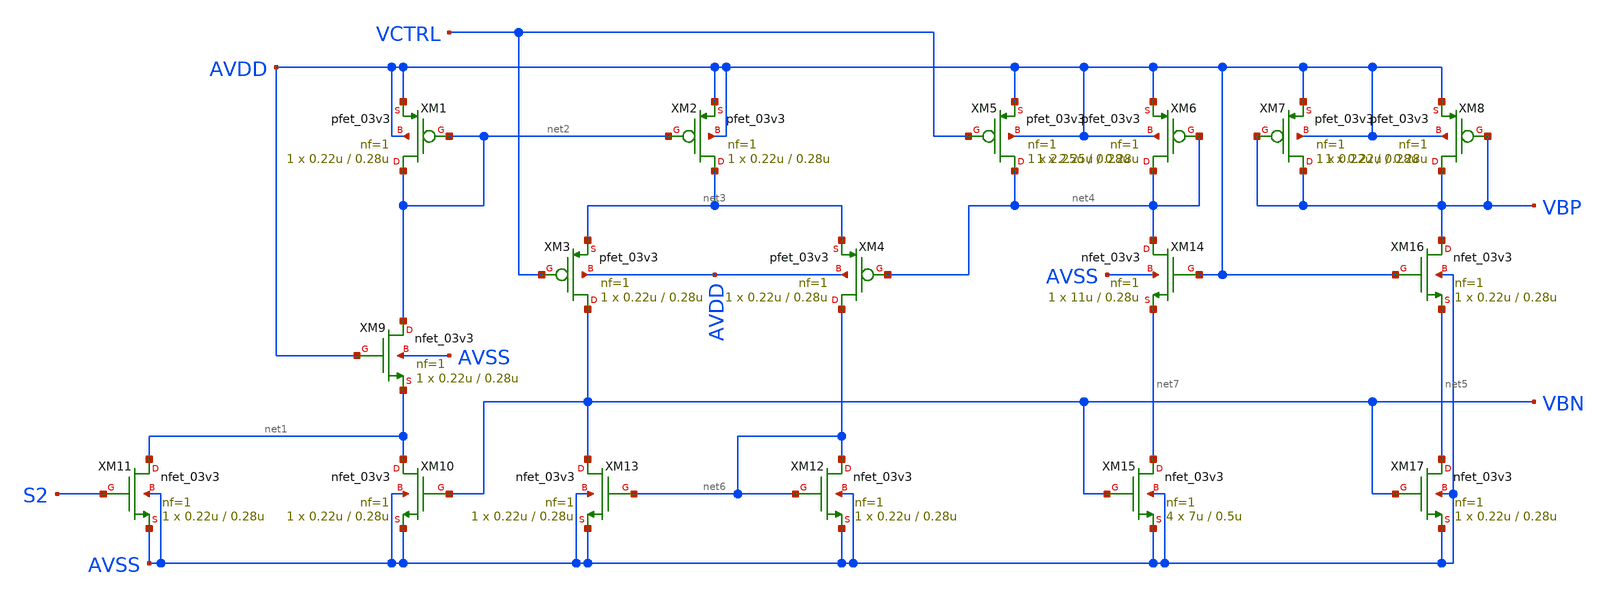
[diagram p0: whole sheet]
** sch_path: designs/libs/core_analog/bias_generator/bias_generator.sch
**.subckt bias_generator
XM1 net2 net2 AVDD AVDD pfet_03v3 L=0.28u W=0.22u nf=1 ad='int((nf+1)/2) * W/nf * 0.18u' as='int((nf+2)/2) * W/nf * 0.18u'
+ pd='2*int((nf+1)/2) * (W/nf + 0.18u)' ps='2*int((nf+2)/2) * (W/nf + 0.18u)' nrd='0.18u / W' nrs='0.18u / W'
+ sa=0 sb=0 sd=0 m=1
XM2 net3 net2 AVDD AVDD pfet_03v3 L=0.28u W=0.22u nf=1 ad='int((nf+1)/2) * W/nf * 0.18u' as='int((nf+2)/2) * W/nf * 0.18u'
+ pd='2*int((nf+1)/2) * (W/nf + 0.18u)' ps='2*int((nf+2)/2) * (W/nf + 0.18u)' nrd='0.18u / W' nrs='0.18u / W'
+ sa=0 sb=0 sd=0 m=1
XM3 VBN VCTRL net3 AVDD pfet_03v3 L=0.28u W=0.22u nf=1 ad='int((nf+1)/2) * W/nf * 0.18u' as='int((nf+2)/2) * W/nf * 0.18u'
+ pd='2*int((nf+1)/2) * (W/nf + 0.18u)' ps='2*int((nf+2)/2) * (W/nf + 0.18u)' nrd='0.18u / W' nrs='0.18u / W'
+ sa=0 sb=0 sd=0 m=1
XM4 net6 net4 net3 AVDD pfet_03v3 L=0.28u W=0.22u nf=1 ad='int((nf+1)/2) * W/nf * 0.18u' as='int((nf+2)/2) * W/nf * 0.18u'
+ pd='2*int((nf+1)/2) * (W/nf + 0.18u)' ps='2*int((nf+2)/2) * (W/nf + 0.18u)' nrd='0.18u / W' nrs='0.18u / W'
+ sa=0 sb=0 sd=0 m=1
XM5 net4 VCTRL AVDD AVDD pfet_03v3 L=0.28u W=2.25u nf=1 ad='int((nf+1)/2) * W/nf * 0.18u' as='int((nf+2)/2) * W/nf * 0.18u'
+ pd='2*int((nf+1)/2) * (W/nf + 0.18u)' ps='2*int((nf+2)/2) * (W/nf + 0.18u)' nrd='0.18u / W' nrs='0.18u / W'
+ sa=0 sb=0 sd=0 m=1
XM7 VBP VBP AVDD AVDD pfet_03v3 L=0.28u W=0.22u nf=1 ad='int((nf+1)/2) * W/nf * 0.18u' as='int((nf+2)/2) * W/nf * 0.18u'
+ pd='2*int((nf+1)/2) * (W/nf + 0.18u)' ps='2*int((nf+2)/2) * (W/nf + 0.18u)' nrd='0.18u / W' nrs='0.18u / W'
+ sa=0 sb=0 sd=0 m=1
XM8 VBP VBP AVDD AVDD pfet_03v3 L=0.28u W=0.22u nf=1 ad='int((nf+1)/2) * W/nf * 0.18u' as='int((nf+2)/2) * W/nf * 0.18u'
+ pd='2*int((nf+1)/2) * (W/nf + 0.18u)' ps='2*int((nf+2)/2) * (W/nf + 0.18u)' nrd='0.18u / W' nrs='0.18u / W'
+ sa=0 sb=0 sd=0 m=1
XM9 net2 AVDD net1 AVSS nfet_03v3 L=0.28u W=0.22u nf=1 ad='int((nf+1)/2) * W/nf * 0.18u' as='int((nf+2)/2) * W/nf * 0.18u'
+ pd='2*int((nf+1)/2) * (W/nf + 0.18u)' ps='2*int((nf+2)/2) * (W/nf + 0.18u)' nrd='0.18u / W' nrs='0.18u / W'
+ sa=0 sb=0 sd=0 m=1
XM10 net1 VBN AVSS AVSS nfet_03v3 L=0.28u W=0.22u nf=1 ad='int((nf+1)/2) * W/nf * 0.18u' as='int((nf+2)/2) * W/nf * 0.18u'
+ pd='2*int((nf+1)/2) * (W/nf + 0.18u)' ps='2*int((nf+2)/2) * (W/nf + 0.18u)' nrd='0.18u / W' nrs='0.18u / W'
+ sa=0 sb=0 sd=0 m=1
XM11 net1 S2 AVSS AVSS nfet_03v3 L=0.28u W=0.22u nf=1 ad='int((nf+1)/2) * W/nf * 0.18u' as='int((nf+2)/2) * W/nf * 0.18u'
+ pd='2*int((nf+1)/2) * (W/nf + 0.18u)' ps='2*int((nf+2)/2) * (W/nf + 0.18u)' nrd='0.18u / W' nrs='0.18u / W'
+ sa=0 sb=0 sd=0 m=1
XM12 net6 net6 AVSS AVSS nfet_03v3 L=0.28u W=0.22u nf=1 ad='int((nf+1)/2) * W/nf * 0.18u' as='int((nf+2)/2) * W/nf * 0.18u'
+ pd='2*int((nf+1)/2) * (W/nf + 0.18u)' ps='2*int((nf+2)/2) * (W/nf + 0.18u)' nrd='0.18u / W' nrs='0.18u / W'
+ sa=0 sb=0 sd=0 m=1
XM13 VBN net6 AVSS AVSS nfet_03v3 L=0.28u W=0.22u nf=1 ad='int((nf+1)/2) * W/nf * 0.18u' as='int((nf+2)/2) * W/nf * 0.18u'
+ pd='2*int((nf+1)/2) * (W/nf + 0.18u)' ps='2*int((nf+2)/2) * (W/nf + 0.18u)' nrd='0.18u / W' nrs='0.18u / W'
+ sa=0 sb=0 sd=0 m=1
XM14 net4 AVDD net7 AVSS nfet_03v3 L=0.28u W=11u nf=1 ad='int((nf+1)/2) * W/nf * 0.18u' as='int((nf+2)/2) * W/nf * 0.18u'
+ pd='2*int((nf+1)/2) * (W/nf + 0.18u)' ps='2*int((nf+2)/2) * (W/nf + 0.18u)' nrd='0.18u / W' nrs='0.18u / W'
+ sa=0 sb=0 sd=0 m=1
XM15 net7 VBN AVSS AVSS nfet_03v3 L=0.5u W=7u nf=1 ad='int((nf+1)/2) * W/nf * 0.18u' as='int((nf+2)/2) * W/nf * 0.18u'
+ pd='2*int((nf+1)/2) * (W/nf + 0.18u)' ps='2*int((nf+2)/2) * (W/nf + 0.18u)' nrd='0.18u / W' nrs='0.18u / W'
+ sa=0 sb=0 sd=0 m=4
XM16 VBP AVDD net5 AVSS nfet_03v3 L=0.28u W=0.22u nf=1 ad='int((nf+1)/2) * W/nf * 0.18u' as='int((nf+2)/2) * W/nf * 0.18u'
+ pd='2*int((nf+1)/2) * (W/nf + 0.18u)' ps='2*int((nf+2)/2) * (W/nf + 0.18u)' nrd='0.18u / W' nrs='0.18u / W'
+ sa=0 sb=0 sd=0 m=1
XM17 net5 VBN AVSS AVSS nfet_03v3 L=0.28u W=0.22u nf=1 ad='int((nf+1)/2) * W/nf * 0.18u' as='int((nf+2)/2) * W/nf * 0.18u'
+ pd='2*int((nf+1)/2) * (W/nf + 0.18u)' ps='2*int((nf+2)/2) * (W/nf + 0.18u)' nrd='0.18u / W' nrs='0.18u / W'
+ sa=0 sb=0 sd=0 m=1
XM6 net4 net4 AVDD AVDD pfet_03v3 L=0.28u W=2.25u nf=1 ad='int((nf+1)/2) * W/nf * 0.18u' as='int((nf+2)/2) * W/nf * 0.18u'
+ pd='2*int((nf+1)/2) * (W/nf + 0.18u)' ps='2*int((nf+2)/2) * (W/nf + 0.18u)' nrd='0.18u / W' nrs='0.18u / W'
+ sa=0 sb=0 sd=0 m=1
**.ends
.end
